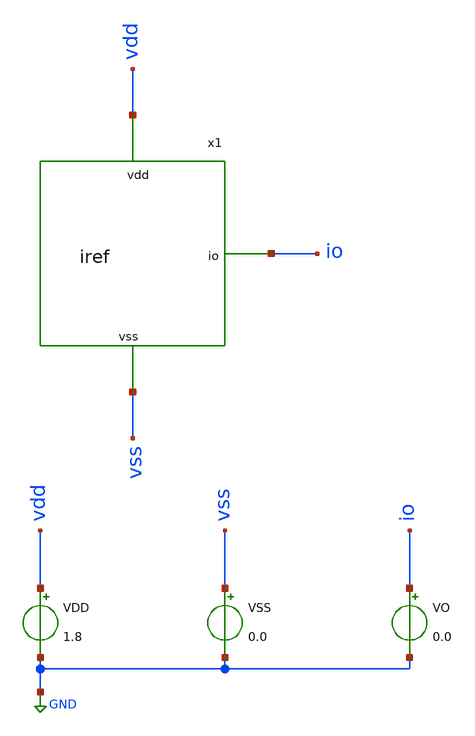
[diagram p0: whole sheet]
** sch_path: xschem/IREF/iref_tb.sch
**.subckt iref_tb
VDD vdd GND 1.8
VSS vss GND 0.0
x1 vdd io vss iref
VO io GND 0.0
**** begin user architecture code



*.include /usr/share/pdk/sky130A/libs.ref/spi/sky130_fd_pr/sky130_fd_pr__pfet_g5v0d10v5__ss.corner.spice
*.include /usr/share/pdk/sky130A/libs.ref/spi/sky130_fd_pr/sky130_fd_pr__pfet_g5v0d10v5__mismatch.corner.spice
*.include /usr/share/pdk/sky130A/libs.ref/spi/sky130_fd_pr/sky130_fd_pr__nfet_g5v0d10v5__tt.corner.spice
*.include /usr/share/pdk/sky130A/libs.ref/spi/sky130_fd_pr/sky130_fd_pr__nfet_g5v0d10v5__mismatch.corner.spice

.include /usr/share/pdk/sky130A/libs.ref/spi/sky130_fd_pr/sky130_fd_pr__nfet_01v8_lvt__tt.corner.spice
.include /usr/share/pdk/sky130A/libs.ref/spi/sky130_fd_pr/sky130_fd_pr__nfet_01v8_lvt__mismatch.corner.spice
.include /usr/share/pdk/sky130A/libs.ref/spi/sky130_fd_pr/sky130_fd_pr__pfet_01v8_lvt__tt.corner.spice
.include /usr/share/pdk/sky130A/libs.ref/spi/sky130_fd_pr/sky130_fd_pr__pfet_01v8_lvt__mismatch.corner.spice

.include ~/OpenPDK/skywater-pdk/skywater-pdk/libraries/sky130_fd_pr/latest/models/all.spice





.param mc_mm_switch=0

.options gmin=1e-12
.options reltol=1e-5
.options abstol=1e-15
*.options rshunt = 1.0e15

.control
  op
  print i(VO)

  dc VDD 0.3 1.8 1m

  let io = i(VO)
  wrdata ../../SIM_DATA/iref_io.txt io
  plot io

  let psrr = deriv(io)/io
  wrdata ../../SIM_DATA/iref_psrr.txt io
  plot ylog abs(psrr)

.endc


**** end user architecture code
**.ends
.GLOBAL GND
.end
